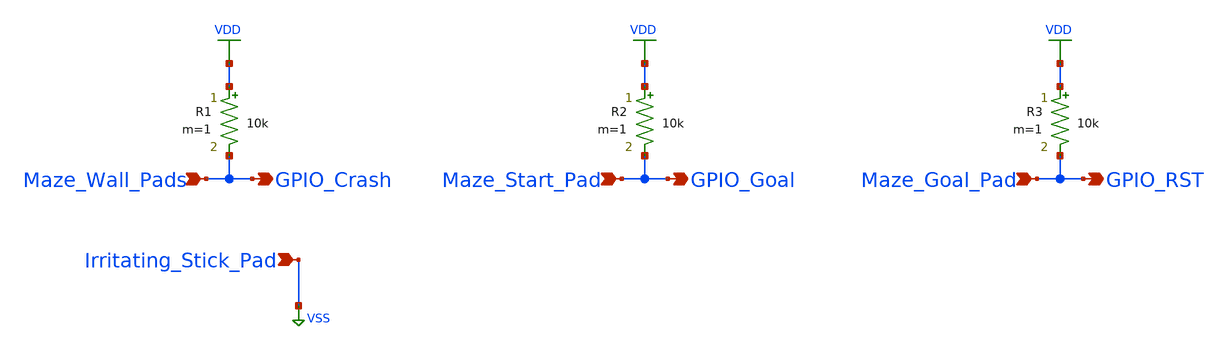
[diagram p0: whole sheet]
** sch_path: xschem/maze.sch
**.subckt maze GPIO_Crash Maze_Start_Pad Maze_Wall_Pads Maze_Goal_Pad GPIO_Goal GPIO_RST
*+ Irritating_Stick_Pad
*.opin GPIO_Crash
*.ipin Maze_Start_Pad
*.ipin Maze_Wall_Pads
*.ipin Maze_Goal_Pad
*.opin GPIO_Goal
*.opin GPIO_RST
*.ipin Irritating_Stick_Pad
R1 VDD GPIO_Crash 10k m=1
R2 VDD Maze_Start_Pad 10k m=1
R3 VDD Maze_Goal_Pad 10k m=1
**.ends
.GLOBAL VDD
.GLOBAL VSS
.end
